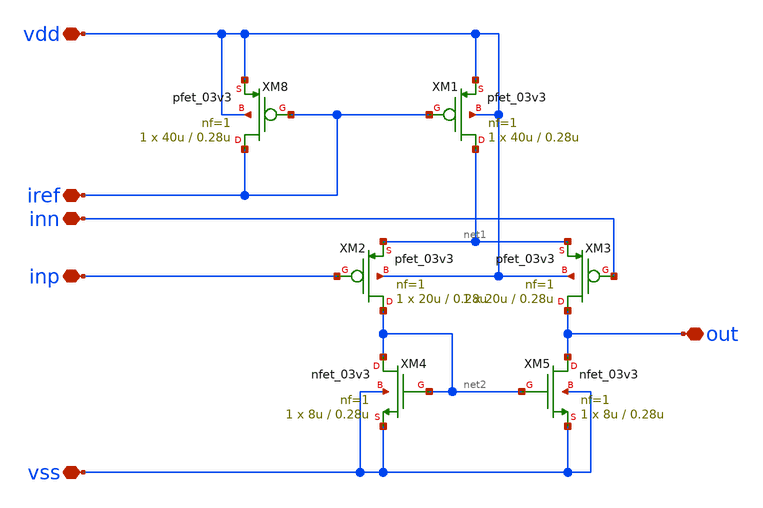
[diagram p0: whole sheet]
** sch_path: designs/libs/qw_core_analog_pkedit/OTAforChargePump/OTAforChargePump.sch
**.subckt OTAforChargePump inp inn vdd vss out iref
*.iopin inp
*.iopin inn
*.iopin vdd
*.iopin vss
*.iopin out
*.iopin iref
XM8 iref iref vdd vdd pfet_03v3 L=0.28u W=40u nf=1 ad='int((nf+1)/2) * W/nf * 0.18u' as='int((nf+2)/2) * W/nf * 0.18u'
+ pd='2*int((nf+1)/2) * (W/nf + 0.18u)' ps='2*int((nf+2)/2) * (W/nf + 0.18u)' nrd='0.18u / W' nrs='0.18u / W'
+ sa=0 sb=0 sd=0 m=1
XM1 net1 iref vdd vdd pfet_03v3 L=0.28u W=40u nf=1 ad='int((nf+1)/2) * W/nf * 0.18u' as='int((nf+2)/2) * W/nf * 0.18u'
+ pd='2*int((nf+1)/2) * (W/nf + 0.18u)' ps='2*int((nf+2)/2) * (W/nf + 0.18u)' nrd='0.18u / W' nrs='0.18u / W'
+ sa=0 sb=0 sd=0 m=1
XM2 net2 inp net1 vdd pfet_03v3 L=0.28u W=20u nf=1 ad='int((nf+1)/2) * W/nf * 0.18u' as='int((nf+2)/2) * W/nf * 0.18u'
+ pd='2*int((nf+1)/2) * (W/nf + 0.18u)' ps='2*int((nf+2)/2) * (W/nf + 0.18u)' nrd='0.18u / W' nrs='0.18u / W'
+ sa=0 sb=0 sd=0 m=1
XM3 out inn net1 vdd pfet_03v3 L=0.28u W=20u nf=1 ad='int((nf+1)/2) * W/nf * 0.18u' as='int((nf+2)/2) * W/nf * 0.18u'
+ pd='2*int((nf+1)/2) * (W/nf + 0.18u)' ps='2*int((nf+2)/2) * (W/nf + 0.18u)' nrd='0.18u / W' nrs='0.18u / W'
+ sa=0 sb=0 sd=0 m=1
XM4 net2 net2 vss vss nfet_03v3 L=0.28u W=8u nf=1 ad='int((nf+1)/2) * W/nf * 0.18u' as='int((nf+2)/2) * W/nf * 0.18u'
+ pd='2*int((nf+1)/2) * (W/nf + 0.18u)' ps='2*int((nf+2)/2) * (W/nf + 0.18u)' nrd='0.18u / W' nrs='0.18u / W'
+ sa=0 sb=0 sd=0 m=1
XM5 out net2 vss vss nfet_03v3 L=0.28u W=8u nf=1 ad='int((nf+1)/2) * W/nf * 0.18u' as='int((nf+2)/2) * W/nf * 0.18u'
+ pd='2*int((nf+1)/2) * (W/nf + 0.18u)' ps='2*int((nf+2)/2) * (W/nf + 0.18u)' nrd='0.18u / W' nrs='0.18u / W'
+ sa=0 sb=0 sd=0 m=1
**.ends
.end
